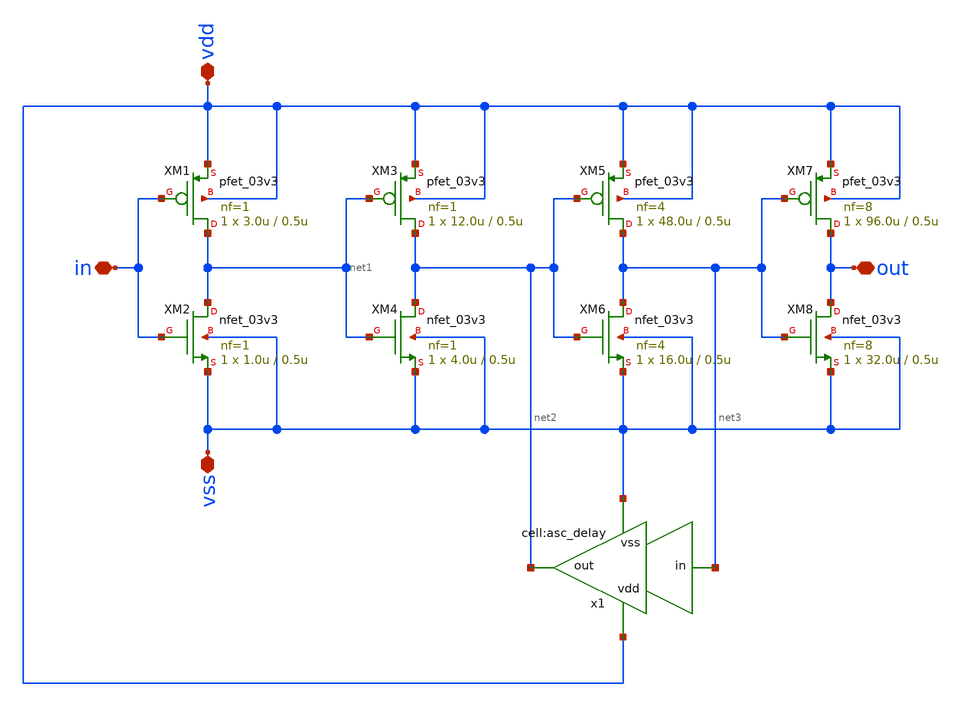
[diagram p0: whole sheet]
** sch_path: designs/libs/core_analog/asc_hysteresis_buffer/asc_hysteresis_buffer.sch
**.subckt asc_hysteresis_buffer in out vss vdd
*.iopin in
*.iopin out
*.iopin vss
*.iopin vdd
XM1 net1 in vdd vdd pfet_03v3 L=0.5u W=3.0u nf=1 ad='int((nf+1)/2) * W/nf * 0.18u' as='int((nf+2)/2) * W/nf * 0.18u'
+ pd='2*int((nf+1)/2) * (W/nf + 0.18u)' ps='2*int((nf+2)/2) * (W/nf + 0.18u)' nrd='0.18u / W' nrs='0.18u / W'
+ sa=0 sb=0 sd=0 m=1
XM2 net1 in vss vss nfet_03v3 L=0.5u W=1.0u nf=1 ad='int((nf+1)/2) * W/nf * 0.18u' as='int((nf+2)/2) * W/nf * 0.18u'
+ pd='2*int((nf+1)/2) * (W/nf + 0.18u)' ps='2*int((nf+2)/2) * (W/nf + 0.18u)' nrd='0.18u / W' nrs='0.18u / W'
+ sa=0 sb=0 sd=0 m=1
XM3 net2 net1 vdd vdd pfet_03v3 L=0.5u W=12.0u nf=1 ad='int((nf+1)/2) * W/nf * 0.18u' as='int((nf+2)/2) * W/nf * 0.18u'
+ pd='2*int((nf+1)/2) * (W/nf + 0.18u)' ps='2*int((nf+2)/2) * (W/nf + 0.18u)' nrd='0.18u / W' nrs='0.18u / W'
+ sa=0 sb=0 sd=0 m=1
XM4 net2 net1 vss vss nfet_03v3 L=0.5u W=4.0u nf=1 ad='int((nf+1)/2) * W/nf * 0.18u' as='int((nf+2)/2) * W/nf * 0.18u'
+ pd='2*int((nf+1)/2) * (W/nf + 0.18u)' ps='2*int((nf+2)/2) * (W/nf + 0.18u)' nrd='0.18u / W' nrs='0.18u / W'
+ sa=0 sb=0 sd=0 m=1
XM5 net3 net2 vdd vdd pfet_03v3 L=0.5u W=48.0u nf=4 ad='int((nf+1)/2) * W/nf * 0.18u' as='int((nf+2)/2) * W/nf * 0.18u'
+ pd='2*int((nf+1)/2) * (W/nf + 0.18u)' ps='2*int((nf+2)/2) * (W/nf + 0.18u)' nrd='0.18u / W' nrs='0.18u / W'
+ sa=0 sb=0 sd=0 m=1
XM6 net3 net2 vss vss nfet_03v3 L=0.5u W=16.0u nf=4 ad='int((nf+1)/2) * W/nf * 0.18u' as='int((nf+2)/2) * W/nf * 0.18u'
+ pd='2*int((nf+1)/2) * (W/nf + 0.18u)' ps='2*int((nf+2)/2) * (W/nf + 0.18u)' nrd='0.18u / W' nrs='0.18u / W'
+ sa=0 sb=0 sd=0 m=1
XM7 out net3 vdd vdd pfet_03v3 L=0.5u W=96.0u nf=8 ad='int((nf+1)/2) * W/nf * 0.18u' as='int((nf+2)/2) * W/nf * 0.18u'
+ pd='2*int((nf+1)/2) * (W/nf + 0.18u)' ps='2*int((nf+2)/2) * (W/nf + 0.18u)' nrd='0.18u / W' nrs='0.18u / W'
+ sa=0 sb=0 sd=0 m=1
XM8 out net3 vss vss nfet_03v3 L=0.5u W=32.0u nf=8 ad='int((nf+1)/2) * W/nf * 0.18u' as='int((nf+2)/2) * W/nf * 0.18u'
+ pd='2*int((nf+1)/2) * (W/nf + 0.18u)' ps='2*int((nf+2)/2) * (W/nf + 0.18u)' nrd='0.18u / W' nrs='0.18u / W'
+ sa=0 sb=0 sd=0 m=1
x1 net3 vss net2 vdd asc_delay
**.ends
.end
